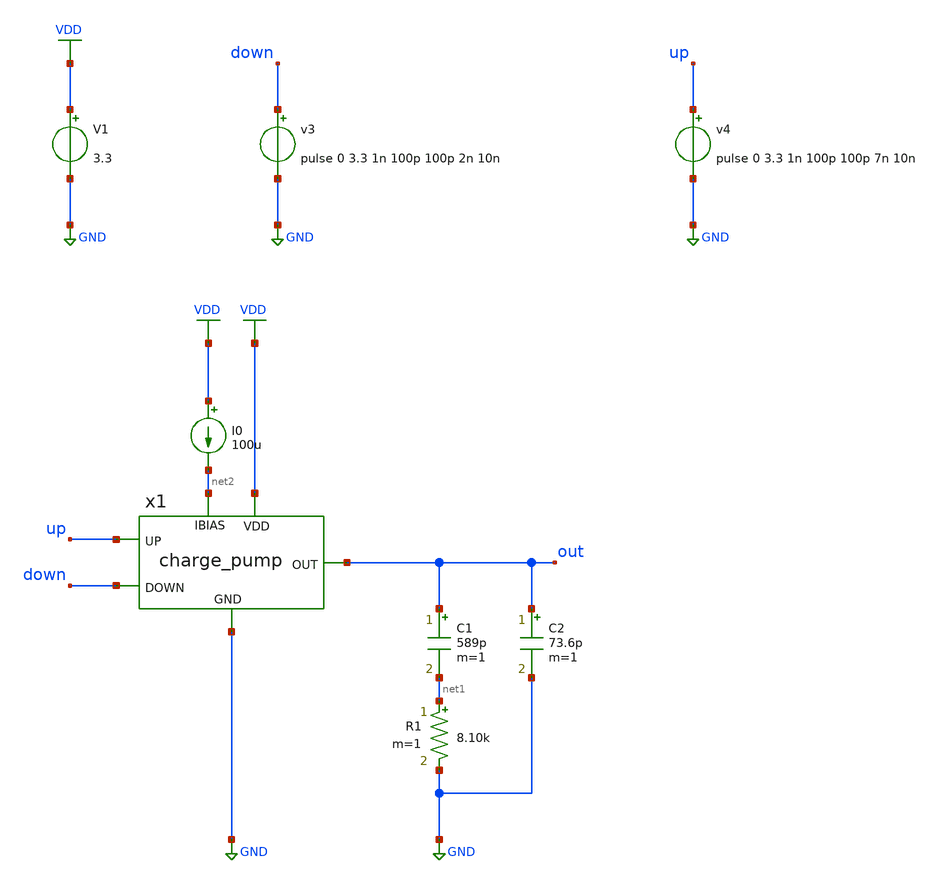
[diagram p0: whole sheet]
** sch_path: designs/libs/tb_analog/tb_charge_pump/tb_charge_pump.sch
**.subckt tb_charge_pump
V1 VDD GND 3.3
R1 net1 GND 8.10k m=1
C1 out net1 589p m=1
C2 out GND 73.6p m=1
v4 up GND pulse 0 3.3 1n 100p 100p 7n 10n
v3 down GND pulse 0 3.3 1n 100p 100p 2n 10n
x1 VDD GND up down out net2 charge_pump
I0 VDD net2 100u
**** begin user architecture code

.include /foss/pdks/gf180mcuD/libs.tech/ngspice/design.ngspice
.lib /foss/pdks/gf180mcuD/libs.tech/ngspice/sm141064.ngspice typical

.option savecurrents

.control
save all
tran 100p 200n
* meas tran IUP_ON AVG i(vmeas1) FROM=50n TO=500n
* meas tran IDOWN_ON AVG i(vmeas2) FROM=50n TO=500n
write tb_charge_pump.raw

.endc

**** end user architecture code
**.ends

* expanding   symbol:  libs/core_analog/charge_pump/charge_pump.sym # of pins=6
** sym_path: designs/libs/core_analog/charge_pump/charge_pump.sym
** sch_path: designs/libs/core_analog/charge_pump/charge_pump.sch
.subckt charge_pump VDD GND UP DOWN OUT IBIAS
*.ipin VDD
*.ipin GND
*.opin OUT
*.ipin IBIAS
*.ipin UP
*.ipin DOWN
XM1 IBIAS IBIAS GND GND nfet_03v3 L=0.28u W=25u nf=1 ad='int((nf+1)/2) * W/nf * 0.18u' as='int((nf+2)/2) * W/nf * 0.18u'
+ pd='2*int((nf+1)/2) * (W/nf + 0.18u)' ps='2*int((nf+2)/2) * (W/nf + 0.18u)' nrd='0.18u / W' nrs='0.18u / W'
+ sa=0 sb=0 sd=0 m=1
XM2 net1 net1 VDD VDD pfet_03v3 L=0.28u W=25u nf=1 ad='int((nf+1)/2) * W/nf * 0.18u' as='int((nf+2)/2) * W/nf * 0.18u'
+ pd='2*int((nf+1)/2) * (W/nf + 0.18u)' ps='2*int((nf+2)/2) * (W/nf + 0.18u)' nrd='0.18u / W' nrs='0.18u / W'
+ sa=0 sb=0 sd=0 m=1
XM4 net4 IBIAS GND GND nfet_03v3 L=0.28u W=25u nf=1 ad='int((nf+1)/2) * W/nf * 0.18u' as='int((nf+2)/2) * W/nf * 0.18u'
+ pd='2*int((nf+1)/2) * (W/nf + 0.18u)' ps='2*int((nf+2)/2) * (W/nf + 0.18u)' nrd='0.18u / W' nrs='0.18u / W'
+ sa=0 sb=0 sd=0 m=1
XM5 net3 net1 VDD VDD pfet_03v3 L=0.28u W=25u nf=1 ad='int((nf+1)/2) * W/nf * 0.18u' as='int((nf+2)/2) * W/nf * 0.18u'
+ pd='2*int((nf+1)/2) * (W/nf + 0.18u)' ps='2*int((nf+2)/2) * (W/nf + 0.18u)' nrd='0.18u / W' nrs='0.18u / W'
+ sa=0 sb=0 sd=0 m=1
XM6 OUT net2 net3 VDD pfet_03v3 L=0.28u W=25u nf=1 ad='int((nf+1)/2) * W/nf * 0.18u' as='int((nf+2)/2) * W/nf * 0.18u'
+ pd='2*int((nf+1)/2) * (W/nf + 0.18u)' ps='2*int((nf+2)/2) * (W/nf + 0.18u)' nrd='0.18u / W' nrs='0.18u / W'
+ sa=0 sb=0 sd=0 m=1
XM7 OUT DOWN net4 GND nfet_03v3 L=0.28u W=25u nf=1 ad='int((nf+1)/2) * W/nf * 0.18u' as='int((nf+2)/2) * W/nf * 0.18u'
+ pd='2*int((nf+1)/2) * (W/nf + 0.18u)' ps='2*int((nf+2)/2) * (W/nf + 0.18u)' nrd='0.18u / W' nrs='0.18u / W'
+ sa=0 sb=0 sd=0 m=1
XM9 net1 IBIAS GND GND nfet_03v3 L=0.28u W=25u nf=1 ad='int((nf+1)/2) * W/nf * 0.18u' as='int((nf+2)/2) * W/nf * 0.18u'
+ pd='2*int((nf+1)/2) * (W/nf + 0.18u)' ps='2*int((nf+2)/2) * (W/nf + 0.18u)' nrd='0.18u / W' nrs='0.18u / W'
+ sa=0 sb=0 sd=0 m=1
XM3 GND UP net2 GND nfet_03v3 L=0.28u W=1u nf=1 ad='int((nf+1)/2) * W/nf * 0.18u' as='int((nf+2)/2) * W/nf * 0.18u'
+ pd='2*int((nf+1)/2) * (W/nf + 0.18u)' ps='2*int((nf+2)/2) * (W/nf + 0.18u)' nrd='0.18u / W' nrs='0.18u / W'
+ sa=0 sb=0 sd=0 m=1
XM8 VDD UP net2 VDD pfet_03v3 L=0.28u W=2u nf=1 ad='int((nf+1)/2) * W/nf * 0.18u' as='int((nf+2)/2) * W/nf * 0.18u'
+ pd='2*int((nf+1)/2) * (W/nf + 0.18u)' ps='2*int((nf+2)/2) * (W/nf + 0.18u)' nrd='0.18u / W' nrs='0.18u / W'
+ sa=0 sb=0 sd=0 m=1
.ends

.GLOBAL GND
.GLOBAL VDD
.end
